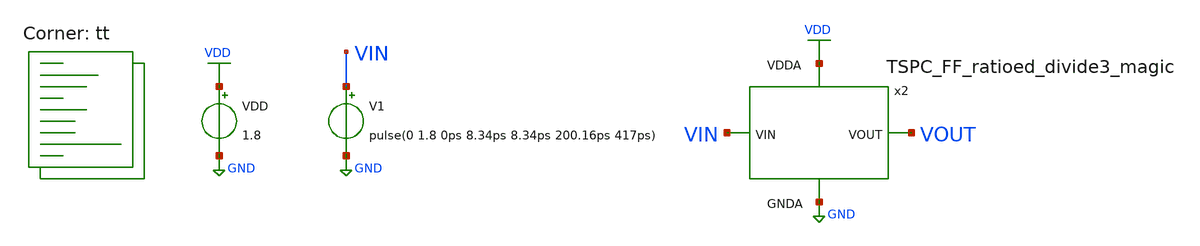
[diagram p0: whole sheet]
** sch_path: projects/pll/divider/magic/divide_by_120/tb_TSPC_FF_ratioed_divide3_magic.sch
**.subckt tb_TSPC_FF_ratioed_divide3_magic
VDD VDD GND 1.8
V1 VIN GND pulse(0 1.8 0ps 8.34ps 8.34ps 200.16ps 417ps)
x2 VOUT VIN VDD GND TSPC_FF_ratioed_divide3_magic
**** begin user architecture code



.include /foss/designs/my_design/projects/pll/divider/magic/divide_by_120/TSPC_FF_ratioed_divide3_magic.spice

.option method=gear
.option wnflag=1

.control

  save all
  tran 2p 10n

  remzerovec
  write tb_TSPC_FF_ratioed_divide3_magic.raw
  set appendwrite

.endc



.lib $::SKYWATER_MODELS/sky130.lib.spice tt
**** end user architecture code
**.ends
.GLOBAL GND
.GLOBAL VDD
.end
